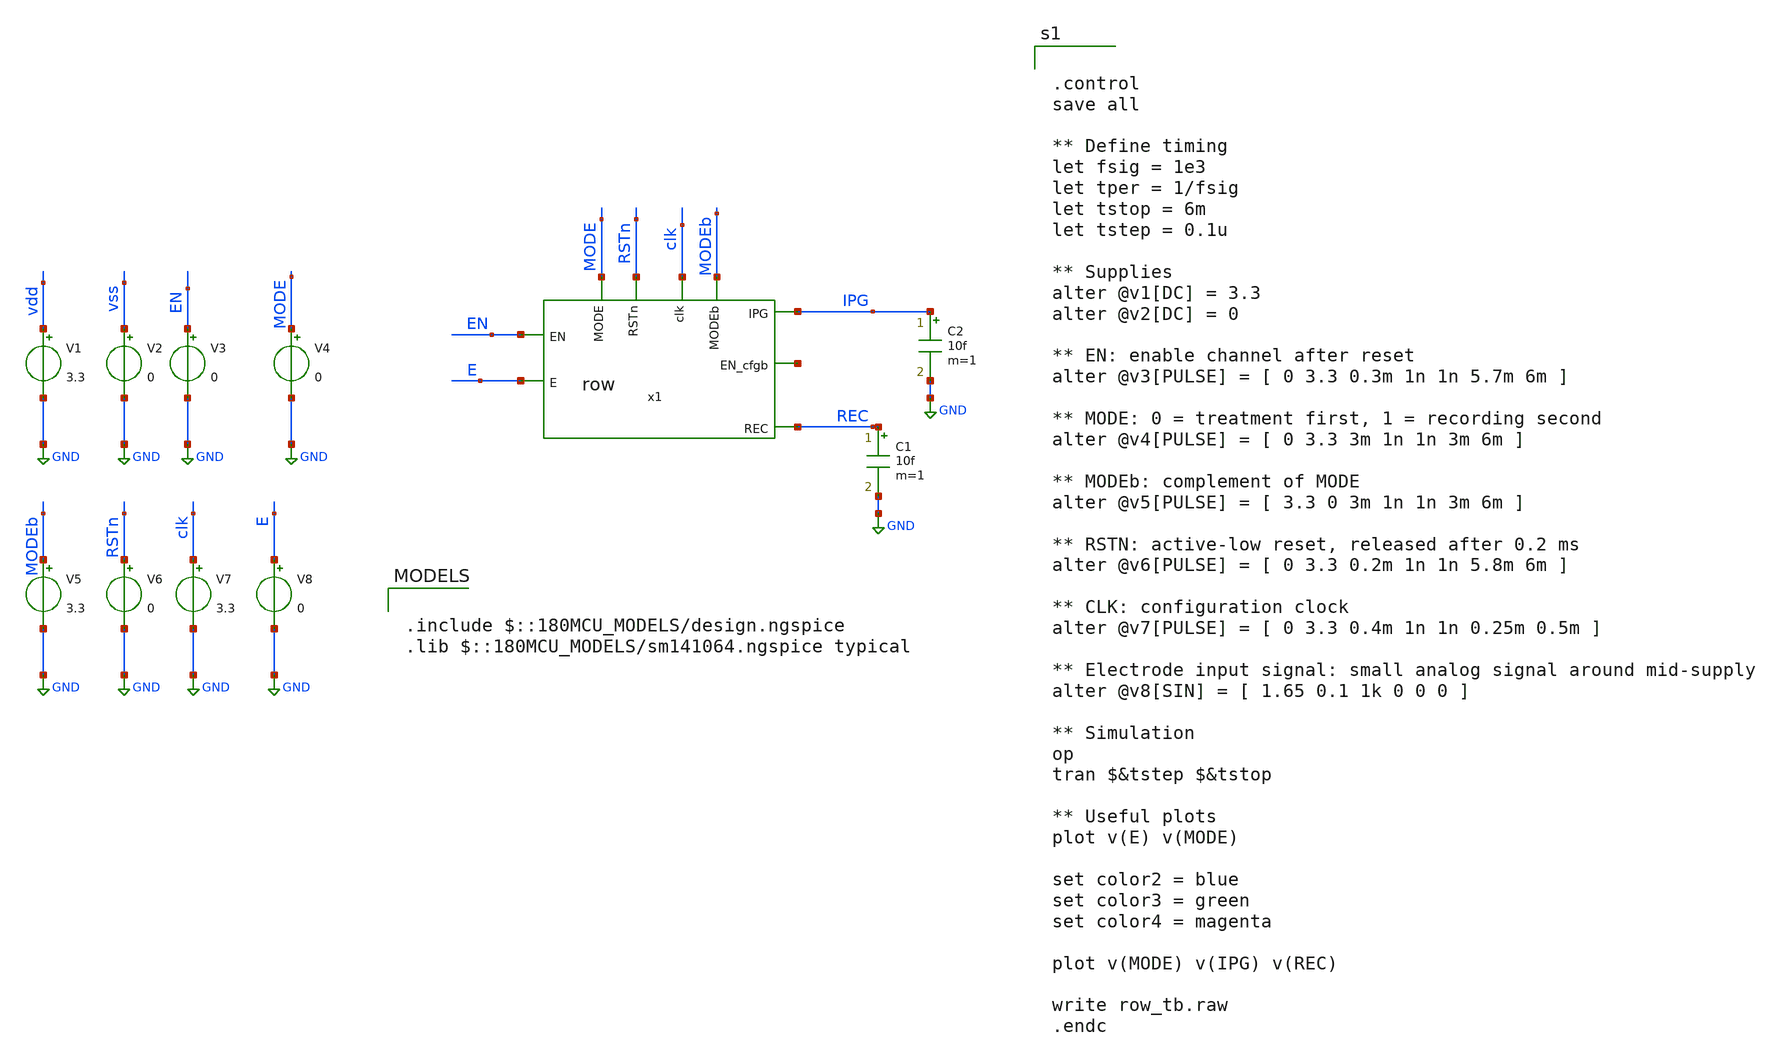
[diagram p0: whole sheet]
** sch_path: row_tb.sch
**.subckt row_tb
x1 IPG MODEb EN net1 clk E MODE RSTn REC row
V1 vdd GND 3.3
V2 vss GND 0
V3 EN GND 0
V4 MODE GND 0
V5 MODEb GND 3.3
V6 RSTn GND 0
V7 clk GND 3.3
V8 E GND 0
C1 REC GND 10f m=1
C2 IPG GND 10f m=1
**** begin user architecture code

.include $::180MCU_MODELS/design.ngspice
.lib $::180MCU_MODELS/sm141064.ngspice typical



.control
save all

** Define timing
let fsig = 1e3
let tper = 1/fsig
let tstop = 6m
let tstep = 0.1u

** Supplies
alter @v1[DC] = 3.3
alter @v2[DC] = 0

** EN: enable channel after reset
alter @v3[PULSE] = [ 0 3.3 0.3m 1n 1n 5.7m 6m ]

** MODE: 0 = treatment first, 1 = recording second
alter @v4[PULSE] = [ 0 3.3 3m 1n 1n 3m 6m ]

** MODEb: complement of MODE
alter @v5[PULSE] = [ 3.3 0 3m 1n 1n 3m 6m ]

** RSTN: active-low reset, released after 0.2 ms
alter @v6[PULSE] = [ 0 3.3 0.2m 1n 1n 5.8m 6m ]

** CLK: configuration clock
alter @v7[PULSE] = [ 0 3.3 0.4m 1n 1n 0.25m 0.5m ]

** Electrode input signal: small analog signal around mid-supply
alter @v8[SIN] = [ 1.65 0.1 1k 0 0 0 ]

** Simulation
op
tran $&tstep $&tstop

** Useful plots
plot v(E) v(MODE)

set color2 = blue
set color3 = green
set color4 = magenta

plot v(MODE) v(IPG) v(REC)

write row_tb.raw
.endc


**** end user architecture code
**.ends

* expanding   symbol:  row.sym # of pins=9
** sym_path: row.sym
** sch_path: row.sch
.subckt row IPG MODEb EN EN_cfgb clk E MODE RSTn REC
*.ipin EN
*.ipin clk
*.ipin MODEb
*.ipin MODE
*.ipin E
*.opin IPG
*.opin REC
*.ipin RSTn
*.opin EN_cfgb
x1 EN_cfg SW_IPG MODEb AND
x2 vdd RSTn EN EN_cfg EN_cfgb clk GND DFF
x3 IPG SW_IPG SW_IPGb E TGATE
x4 EN_cfg SW_REC MODE AND
x6 REC SW_REC SW_RECb E TGATE
x5 SW_IPGb SW_IPG INV
x7 SW_RECb SW_REC INV
.ends


* expanding   symbol:  AND/AND.sym # of pins=3
** sym_path: AND/AND.sym
** sch_path: AND/AND.sch
.subckt AND IN0 OUT IN1
*.opin OUT
*.ipin IN0
*.ipin IN1
XM1 net1 IN0 net2 GND nfet_03v3 L=0.28u W=1u nf=1 ad='int((nf+1)/2) * W/nf * 0.18u' as='int((nf+2)/2) * W/nf * 0.18u'
+ pd='2*int((nf+1)/2) * (W/nf + 0.18u)' ps='2*int((nf+2)/2) * (W/nf + 0.18u)' nrd='0.18u / W' nrs='0.18u / W'
+ sa=0 sb=0 sd=0 m=1
XM2 net2 IN1 GND GND nfet_03v3 L=0.28u W=1u nf=1 ad='int((nf+1)/2) * W/nf * 0.18u' as='int((nf+2)/2) * W/nf * 0.18u'
+ pd='2*int((nf+1)/2) * (W/nf + 0.18u)' ps='2*int((nf+2)/2) * (W/nf + 0.18u)' nrd='0.18u / W' nrs='0.18u / W'
+ sa=0 sb=0 sd=0 m=1
XM3 net1 IN0 vdd vdd pfet_03v3 L=0.28u W=1u nf=1 ad='int((nf+1)/2) * W/nf * 0.18u' as='int((nf+2)/2) * W/nf * 0.18u'
+ pd='2*int((nf+1)/2) * (W/nf + 0.18u)' ps='2*int((nf+2)/2) * (W/nf + 0.18u)' nrd='0.18u / W' nrs='0.18u / W'
+ sa=0 sb=0 sd=0 m=1
XM4 net1 IN1 vdd vdd pfet_03v3 L=0.28u W=1u nf=1 ad='int((nf+1)/2) * W/nf * 0.18u' as='int((nf+2)/2) * W/nf * 0.18u'
+ pd='2*int((nf+1)/2) * (W/nf + 0.18u)' ps='2*int((nf+2)/2) * (W/nf + 0.18u)' nrd='0.18u / W' nrs='0.18u / W'
+ sa=0 sb=0 sd=0 m=1
x1 OUT net1 INV
.ends


* expanding   symbol:  DFF/DFF.sym # of pins=7
** sym_path: DFF/DFF.sym
** sch_path: DFF/DFF.sch
.subckt DFF vdd RSTn D Q Qb CLK vss
*.ipin D
*.ipin CLK
*.ipin RSTn
*.opin Q
*.iopin vdd
*.iopin vss
*.opin Qb
XM1 net1 D net3 vss nfet_03v3 L=0.28u W=1u nf=1 ad='int((nf+1)/2) * W/nf * 0.18u' as='int((nf+2)/2) * W/nf * 0.18u'
+ pd='2*int((nf+1)/2) * (W/nf + 0.18u)' ps='2*int((nf+2)/2) * (W/nf + 0.18u)' nrd='0.18u / W' nrs='0.18u / W'
+ sa=0 sb=0 sd=0 m=1
XM2 net1 D net2 vdd pfet_03v3 L=0.28u W=1u nf=1 ad='int((nf+1)/2) * W/nf * 0.18u' as='int((nf+2)/2) * W/nf * 0.18u'
+ pd='2*int((nf+1)/2) * (W/nf + 0.18u)' ps='2*int((nf+2)/2) * (W/nf + 0.18u)' nrd='0.18u / W' nrs='0.18u / W'
+ sa=0 sb=0 sd=0 m=1
XM3 net2 c vdd vdd pfet_03v3 L=0.28u W=1u nf=1 ad='int((nf+1)/2) * W/nf * 0.18u' as='int((nf+2)/2) * W/nf * 0.18u'
+ pd='2*int((nf+1)/2) * (W/nf + 0.18u)' ps='2*int((nf+2)/2) * (W/nf + 0.18u)' nrd='0.18u / W' nrs='0.18u / W'
+ sa=0 sb=0 sd=0 m=1
XM4 net3 cbar vss vss nfet_03v3 L=0.28u W=1u nf=1 ad='int((nf+1)/2) * W/nf * 0.18u' as='int((nf+2)/2) * W/nf * 0.18u'
+ pd='2*int((nf+1)/2) * (W/nf + 0.18u)' ps='2*int((nf+2)/2) * (W/nf + 0.18u)' nrd='0.18u / W' nrs='0.18u / W'
+ sa=0 sb=0 sd=0 m=1
XM5 cbar CLK vss vss nfet_03v3 L=0.28u W=1u nf=1 ad='int((nf+1)/2) * W/nf * 0.18u' as='int((nf+2)/2) * W/nf * 0.18u'
+ pd='2*int((nf+1)/2) * (W/nf + 0.18u)' ps='2*int((nf+2)/2) * (W/nf + 0.18u)' nrd='0.18u / W' nrs='0.18u / W'
+ sa=0 sb=0 sd=0 m=1
XM6 cbar CLK vdd vdd pfet_03v3 L=0.28u W=1u nf=1 ad='int((nf+1)/2) * W/nf * 0.18u' as='int((nf+2)/2) * W/nf * 0.18u'
+ pd='2*int((nf+1)/2) * (W/nf + 0.18u)' ps='2*int((nf+2)/2) * (W/nf + 0.18u)' nrd='0.18u / W' nrs='0.18u / W'
+ sa=0 sb=0 sd=0 m=1
XM7 c cbar vss vss nfet_03v3 L=0.28u W=1u nf=1 ad='int((nf+1)/2) * W/nf * 0.18u' as='int((nf+2)/2) * W/nf * 0.18u'
+ pd='2*int((nf+1)/2) * (W/nf + 0.18u)' ps='2*int((nf+2)/2) * (W/nf + 0.18u)' nrd='0.18u / W' nrs='0.18u / W'
+ sa=0 sb=0 sd=0 m=1
XM8 c cbar vdd vdd pfet_03v3 L=0.28u W=1u nf=1 ad='int((nf+1)/2) * W/nf * 0.18u' as='int((nf+2)/2) * W/nf * 0.18u'
+ pd='2*int((nf+1)/2) * (W/nf + 0.18u)' ps='2*int((nf+2)/2) * (W/nf + 0.18u)' nrd='0.18u / W' nrs='0.18u / W'
+ sa=0 sb=0 sd=0 m=1
XM11 net5 RSTn net4 vss nfet_03v3 L=0.28u W=1u nf=1 ad='int((nf+1)/2) * W/nf * 0.18u' as='int((nf+2)/2) * W/nf * 0.18u'
+ pd='2*int((nf+1)/2) * (W/nf + 0.18u)' ps='2*int((nf+2)/2) * (W/nf + 0.18u)' nrd='0.18u / W' nrs='0.18u / W'
+ sa=0 sb=0 sd=0 m=1
XM12 net4 net6 vss vss nfet_03v3 L=0.28u W=1u nf=1 ad='int((nf+1)/2) * W/nf * 0.18u' as='int((nf+2)/2) * W/nf * 0.18u'
+ pd='2*int((nf+1)/2) * (W/nf + 0.18u)' ps='2*int((nf+2)/2) * (W/nf + 0.18u)' nrd='0.18u / W' nrs='0.18u / W'
+ sa=0 sb=0 sd=0 m=1
XM13 net5 RSTn vdd vdd pfet_03v3 L=0.28u W=1u nf=1 ad='int((nf+1)/2) * W/nf * 0.18u' as='int((nf+2)/2) * W/nf * 0.18u'
+ pd='2*int((nf+1)/2) * (W/nf + 0.18u)' ps='2*int((nf+2)/2) * (W/nf + 0.18u)' nrd='0.18u / W' nrs='0.18u / W'
+ sa=0 sb=0 sd=0 m=1
XM14 net5 net6 vdd vdd pfet_03v3 L=0.28u W=1u nf=1 ad='int((nf+1)/2) * W/nf * 0.18u' as='int((nf+2)/2) * W/nf * 0.18u'
+ pd='2*int((nf+1)/2) * (W/nf + 0.18u)' ps='2*int((nf+2)/2) * (W/nf + 0.18u)' nrd='0.18u / W' nrs='0.18u / W'
+ sa=0 sb=0 sd=0 m=1
XM15 net6 net1 vss vss nfet_03v3 L=0.28u W=1u nf=1 ad='int((nf+1)/2) * W/nf * 0.18u' as='int((nf+2)/2) * W/nf * 0.18u'
+ pd='2*int((nf+1)/2) * (W/nf + 0.18u)' ps='2*int((nf+2)/2) * (W/nf + 0.18u)' nrd='0.18u / W' nrs='0.18u / W'
+ sa=0 sb=0 sd=0 m=1
XM16 net6 net1 vdd vdd pfet_03v3 L=0.28u W=1u nf=1 ad='int((nf+1)/2) * W/nf * 0.18u' as='int((nf+2)/2) * W/nf * 0.18u'
+ pd='2*int((nf+1)/2) * (W/nf + 0.18u)' ps='2*int((nf+2)/2) * (W/nf + 0.18u)' nrd='0.18u / W' nrs='0.18u / W'
+ sa=0 sb=0 sd=0 m=1
XM21 net9 net7 net8 vss nfet_03v3 L=0.28u W=1u nf=1 ad='int((nf+1)/2) * W/nf * 0.18u' as='int((nf+2)/2) * W/nf * 0.18u'
+ pd='2*int((nf+1)/2) * (W/nf + 0.18u)' ps='2*int((nf+2)/2) * (W/nf + 0.18u)' nrd='0.18u / W' nrs='0.18u / W'
+ sa=0 sb=0 sd=0 m=1
XM22 net8 RSTn vss vss nfet_03v3 L=0.28u W=1u nf=1 ad='int((nf+1)/2) * W/nf * 0.18u' as='int((nf+2)/2) * W/nf * 0.18u'
+ pd='2*int((nf+1)/2) * (W/nf + 0.18u)' ps='2*int((nf+2)/2) * (W/nf + 0.18u)' nrd='0.18u / W' nrs='0.18u / W'
+ sa=0 sb=0 sd=0 m=1
XM23 net9 net7 vdd vdd pfet_03v3 L=0.28u W=1u nf=1 ad='int((nf+1)/2) * W/nf * 0.18u' as='int((nf+2)/2) * W/nf * 0.18u'
+ pd='2*int((nf+1)/2) * (W/nf + 0.18u)' ps='2*int((nf+2)/2) * (W/nf + 0.18u)' nrd='0.18u / W' nrs='0.18u / W'
+ sa=0 sb=0 sd=0 m=1
XM24 net9 RSTn vdd vdd pfet_03v3 L=0.28u W=1u nf=1 ad='int((nf+1)/2) * W/nf * 0.18u' as='int((nf+2)/2) * W/nf * 0.18u'
+ pd='2*int((nf+1)/2) * (W/nf + 0.18u)' ps='2*int((nf+2)/2) * (W/nf + 0.18u)' nrd='0.18u / W' nrs='0.18u / W'
+ sa=0 sb=0 sd=0 m=1
XM25 Q net9 vss vss nfet_03v3 L=0.28u W=1u nf=1 ad='int((nf+1)/2) * W/nf * 0.18u' as='int((nf+2)/2) * W/nf * 0.18u'
+ pd='2*int((nf+1)/2) * (W/nf + 0.18u)' ps='2*int((nf+2)/2) * (W/nf + 0.18u)' nrd='0.18u / W' nrs='0.18u / W'
+ sa=0 sb=0 sd=0 m=1
XM26 Q net9 vdd vdd pfet_03v3 L=0.28u W=1u nf=1 ad='int((nf+1)/2) * W/nf * 0.18u' as='int((nf+2)/2) * W/nf * 0.18u'
+ pd='2*int((nf+1)/2) * (W/nf + 0.18u)' ps='2*int((nf+2)/2) * (W/nf + 0.18u)' nrd='0.18u / W' nrs='0.18u / W'
+ sa=0 sb=0 sd=0 m=1
XM19 net7 net9 net11 vss nfet_03v3 L=0.28u W=1u nf=1 ad='int((nf+1)/2) * W/nf * 0.18u' as='int((nf+2)/2) * W/nf * 0.18u'
+ pd='2*int((nf+1)/2) * (W/nf + 0.18u)' ps='2*int((nf+2)/2) * (W/nf + 0.18u)' nrd='0.18u / W' nrs='0.18u / W'
+ sa=0 sb=0 sd=0 m=1
XM20 net7 net9 net10 vdd pfet_03v3 L=0.28u W=1u nf=1 ad='int((nf+1)/2) * W/nf * 0.18u' as='int((nf+2)/2) * W/nf * 0.18u'
+ pd='2*int((nf+1)/2) * (W/nf + 0.18u)' ps='2*int((nf+2)/2) * (W/nf + 0.18u)' nrd='0.18u / W' nrs='0.18u / W'
+ sa=0 sb=0 sd=0 m=1
XM31 net10 c vdd vdd pfet_03v3 L=0.28u W=1u nf=1 ad='int((nf+1)/2) * W/nf * 0.18u' as='int((nf+2)/2) * W/nf * 0.18u'
+ pd='2*int((nf+1)/2) * (W/nf + 0.18u)' ps='2*int((nf+2)/2) * (W/nf + 0.18u)' nrd='0.18u / W' nrs='0.18u / W'
+ sa=0 sb=0 sd=0 m=1
XM32 net11 cbar vss vss nfet_03v3 L=0.28u W=1u nf=1 ad='int((nf+1)/2) * W/nf * 0.18u' as='int((nf+2)/2) * W/nf * 0.18u'
+ pd='2*int((nf+1)/2) * (W/nf + 0.18u)' ps='2*int((nf+2)/2) * (W/nf + 0.18u)' nrd='0.18u / W' nrs='0.18u / W'
+ sa=0 sb=0 sd=0 m=1
XM35 net12 net9 vss vss nfet_03v3 L=0.28u W=1u nf=1 ad='int((nf+1)/2) * W/nf * 0.18u' as='int((nf+2)/2) * W/nf * 0.18u'
+ pd='2*int((nf+1)/2) * (W/nf + 0.18u)' ps='2*int((nf+2)/2) * (W/nf + 0.18u)' nrd='0.18u / W' nrs='0.18u / W'
+ sa=0 sb=0 sd=0 m=1
XM36 net12 net9 vdd vdd pfet_03v3 L=0.28u W=1u nf=1 ad='int((nf+1)/2) * W/nf * 0.18u' as='int((nf+2)/2) * W/nf * 0.18u'
+ pd='2*int((nf+1)/2) * (W/nf + 0.18u)' ps='2*int((nf+2)/2) * (W/nf + 0.18u)' nrd='0.18u / W' nrs='0.18u / W'
+ sa=0 sb=0 sd=0 m=1
XM37 Qb net12 vss vss nfet_03v3 L=0.28u W=1u nf=1 ad='int((nf+1)/2) * W/nf * 0.18u' as='int((nf+2)/2) * W/nf * 0.18u'
+ pd='2*int((nf+1)/2) * (W/nf + 0.18u)' ps='2*int((nf+2)/2) * (W/nf + 0.18u)' nrd='0.18u / W' nrs='0.18u / W'
+ sa=0 sb=0 sd=0 m=1
XM38 Qb net12 vdd vdd pfet_03v3 L=0.28u W=1u nf=1 ad='int((nf+1)/2) * W/nf * 0.18u' as='int((nf+2)/2) * W/nf * 0.18u'
+ pd='2*int((nf+1)/2) * (W/nf + 0.18u)' ps='2*int((nf+2)/2) * (W/nf + 0.18u)' nrd='0.18u / W' nrs='0.18u / W'
+ sa=0 sb=0 sd=0 m=1
XM9 net1 c net5 vss nfet_03v3 L=0.28u W=1u nf=1 ad='int((nf+1)/2) * W/nf * 0.18u' as='int((nf+2)/2) * W/nf * 0.18u'
+ pd='2*int((nf+1)/2) * (W/nf + 0.18u)' ps='2*int((nf+2)/2) * (W/nf + 0.18u)' nrd='0.18u / W' nrs='0.18u / W'
+ sa=0 sb=0 sd=0 m=1
XM10 net1 cbar net5 vdd pfet_03v3 L=0.28u W=1u nf=1 ad='int((nf+1)/2) * W/nf * 0.18u' as='int((nf+2)/2) * W/nf * 0.18u'
+ pd='2*int((nf+1)/2) * (W/nf + 0.18u)' ps='2*int((nf+2)/2) * (W/nf + 0.18u)' nrd='0.18u / W' nrs='0.18u / W'
+ sa=0 sb=0 sd=0 m=1
XM17 net6 c net7 vss nfet_03v3 L=0.28u W=1u nf=1 ad='int((nf+1)/2) * W/nf * 0.18u' as='int((nf+2)/2) * W/nf * 0.18u'
+ pd='2*int((nf+1)/2) * (W/nf + 0.18u)' ps='2*int((nf+2)/2) * (W/nf + 0.18u)' nrd='0.18u / W' nrs='0.18u / W'
+ sa=0 sb=0 sd=0 m=1
XM18 net6 cbar net7 vdd pfet_03v3 L=0.28u W=1u nf=1 ad='int((nf+1)/2) * W/nf * 0.18u' as='int((nf+2)/2) * W/nf * 0.18u'
+ pd='2*int((nf+1)/2) * (W/nf + 0.18u)' ps='2*int((nf+2)/2) * (W/nf + 0.18u)' nrd='0.18u / W' nrs='0.18u / W'
+ sa=0 sb=0 sd=0 m=1
.ends


* expanding   symbol:  TGATE/TGATE.sym # of pins=4
** sym_path: TGATE/TGATE.sym
** sch_path: TGATE/TGATE.sch
.subckt TGATE out c cbar in
*.ipin in
*.opin out
*.ipin cbar
*.ipin c
XM1 out cbar in VDD pfet_03v3 L=0.28u W=1u nf=1 ad='int((nf+1)/2) * W/nf * 0.18u' as='int((nf+2)/2) * W/nf * 0.18u'
+ pd='2*int((nf+1)/2) * (W/nf + 0.18u)' ps='2*int((nf+2)/2) * (W/nf + 0.18u)' nrd='0.18u / W' nrs='0.18u / W'
+ sa=0 sb=0 sd=0 m=1
XM2 out c in GND nfet_03v3 L=0.28u W=1u nf=1 ad='int((nf+1)/2) * W/nf * 0.18u' as='int((nf+2)/2) * W/nf * 0.18u'
+ pd='2*int((nf+1)/2) * (W/nf + 0.18u)' ps='2*int((nf+2)/2) * (W/nf + 0.18u)' nrd='0.18u / W' nrs='0.18u / W'
+ sa=0 sb=0 sd=0 m=1
.ends


* expanding   symbol:  AND/INV.sym # of pins=2
** sym_path: AND/INV.sym
** sch_path: AND/INV.sch
.subckt INV OUT IN
*.ipin IN
*.opin OUT
XM1 OUT IN VDD VDD pfet_03v3 L=0.28u W=1u nf=1 ad='int((nf+1)/2) * W/nf * 0.18u' as='int((nf+2)/2) * W/nf * 0.18u'
+ pd='2*int((nf+1)/2) * (W/nf + 0.18u)' ps='2*int((nf+2)/2) * (W/nf + 0.18u)' nrd='0.18u / W' nrs='0.18u / W'
+ sa=0 sb=0 sd=0 m=1
XM2 OUT IN GND GND nfet_03v3 L=0.28u W=0.5u nf=1 ad='int((nf+1)/2) * W/nf * 0.18u' as='int((nf+2)/2) * W/nf * 0.18u'
+ pd='2*int((nf+1)/2) * (W/nf + 0.18u)' ps='2*int((nf+2)/2) * (W/nf + 0.18u)' nrd='0.18u / W' nrs='0.18u / W'
+ sa=0 sb=0 sd=0 m=1
.ends

.GLOBAL GND
.GLOBAL vdd
.GLOBAL VDD
.end
